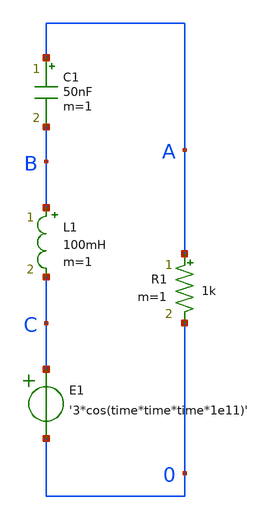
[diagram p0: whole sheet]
** sch_path: BTDay1-Ex/Ex1_Lecture1.sch
**.subckt Ex1_Lecture1
R1 A 0 1k m=1
C1 A B 50nF m=1
L1 B C 100mH m=1
E1 C 0 VOL=' '3*cos(time*time*time*1e11)' '
**** begin user architecture code

.tran 10n 2000u uic
.save all

**** end user architecture code
**.ends
.end
